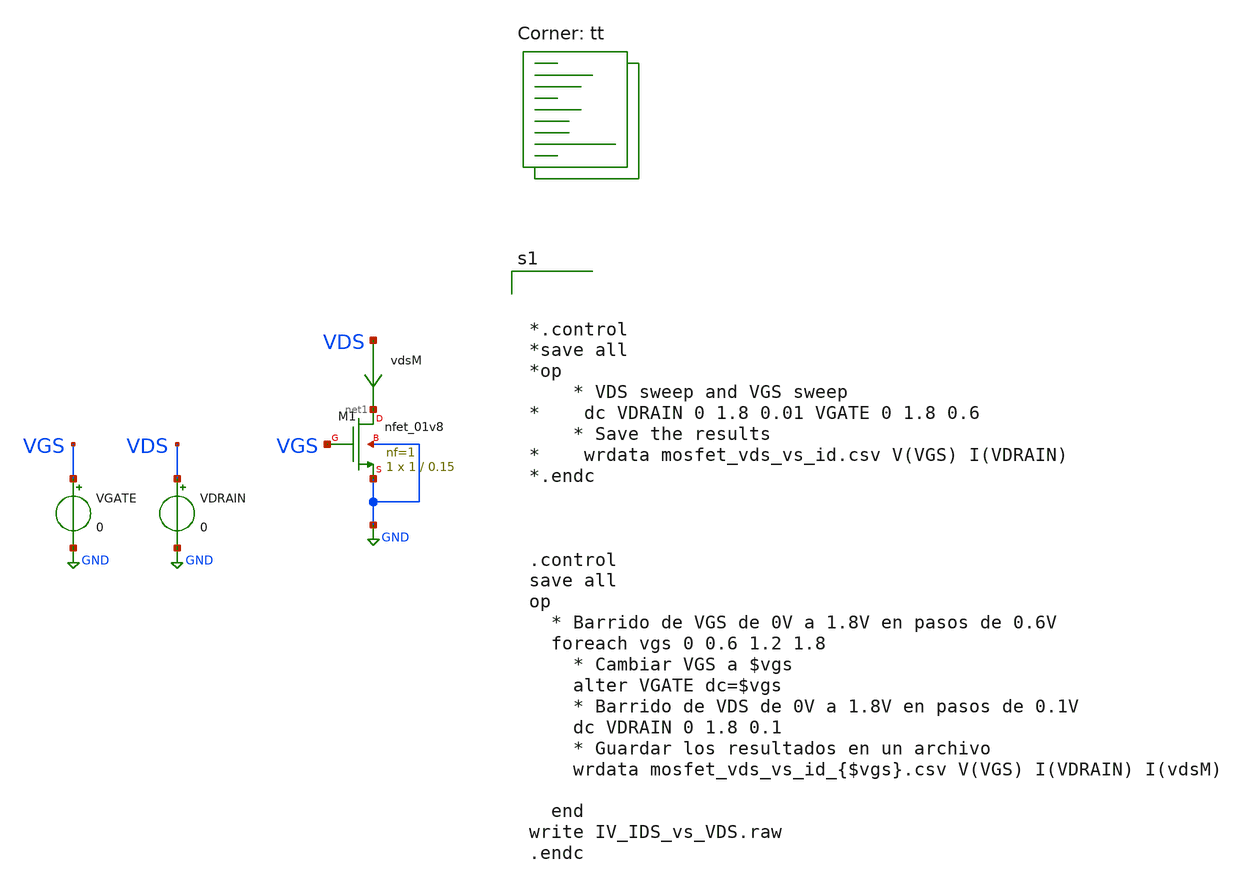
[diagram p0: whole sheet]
** sch_path: circuits/copys_to_develop_pmos/IV_IDS_vs_VDS.sch
**.subckt IV_IDS_vs_VDS
XM1 net1 VGS GND GND sky130_fd_pr__nfet_01v8 L=0.15 W=1 nf=1 ad='int((nf+1)/2) * W/nf * 0.29' as='int((nf+2)/2) * W/nf * 0.29'
+ pd='2*int((nf+1)/2) * (W/nf + 0.29)' ps='2*int((nf+2)/2) * (W/nf + 0.29)' nrd='0.29 / W' nrs='0.29 / W'
+ sa=0 sb=0 sd=0 mult=1 m=1
VGATE VGS GND 0
VDRAIN VDS GND 0
vdsM VDS net1 0
.save i(vdsm)
**** begin user architecture code



*.control
*save all
*op
    * VDS sweep and VGS sweep
*    dc VDRAIN 0 1.8 0.01 VGATE 0 1.8 0.6
    * Save the results
*    wrdata mosfet_vds_vs_id.csv V(VGS) I(VDRAIN)
*.endc



.control
save all
op
  * Barrido de VGS de 0V a 1.8V en pasos de 0.6V
  foreach vgs 0 0.6 1.2 1.8
    * Cambiar VGS a $vgs
    alter VGATE dc=$vgs
    * Barrido de VDS de 0V a 1.8V en pasos de 0.1V
    dc VDRAIN 0 1.8 0.1
    * Guardar los resultados en un archivo
    wrdata mosfet_vds_vs_id_{$vgs}.csv V(VGS) I(VDRAIN) I(vdsM)

  end
write IV_IDS_vs_VDS.raw
.endc



.lib $::SKYWATER_MODELS/sky130.lib.spice tt
**** end user architecture code
**.ends
.GLOBAL GND
.end
